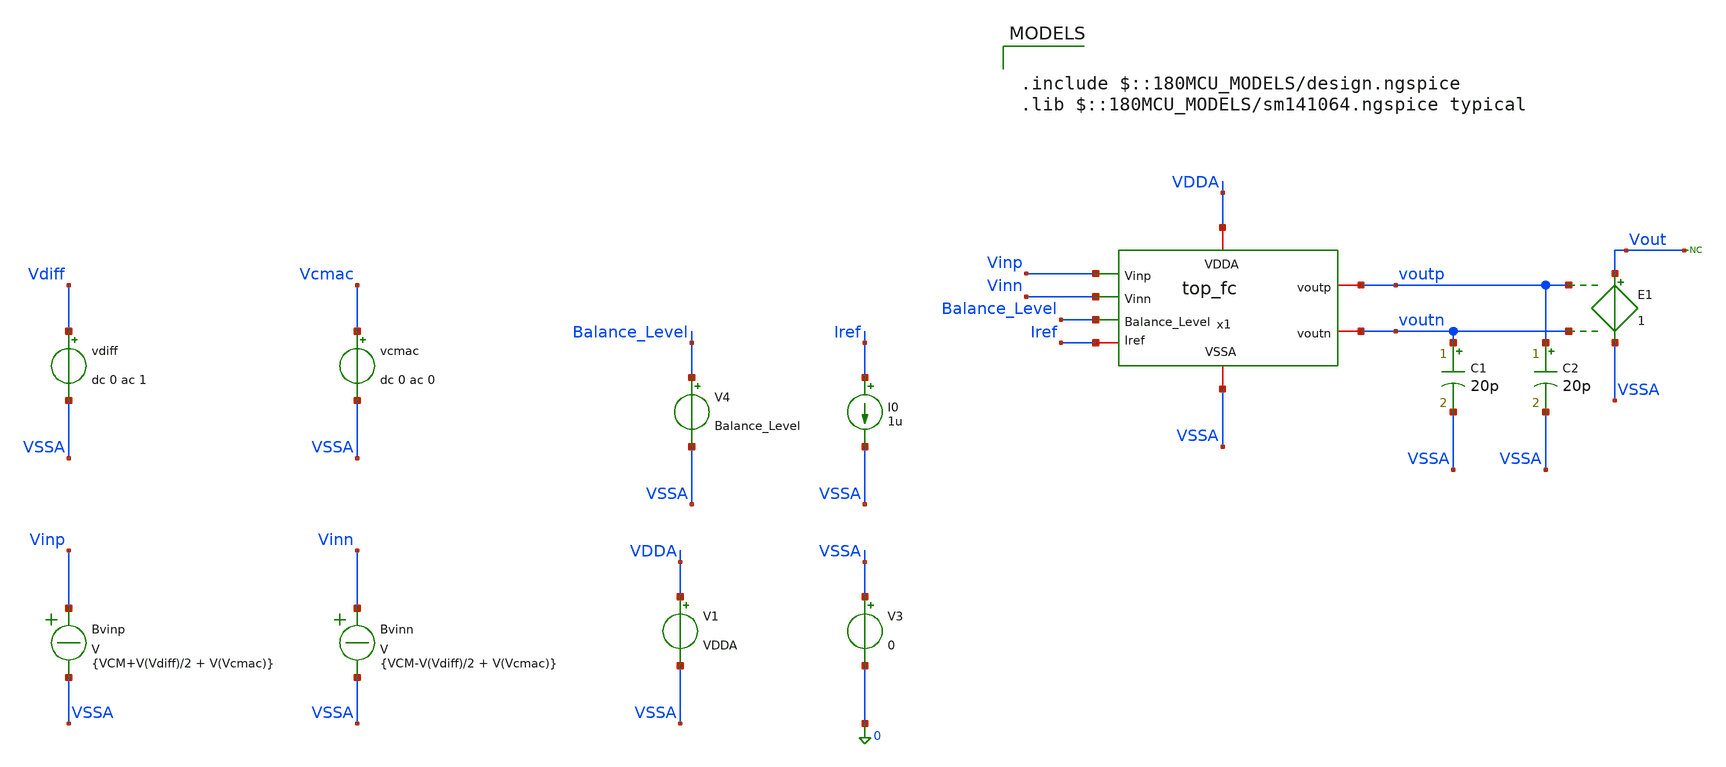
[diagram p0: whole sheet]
** sch_path: Folded_cascode/testbenches/top_fc_cmrr_tb.sch
**.subckt top_fc_cmrr_tb
x1 Balance_Level Vinp voutp VDDA voutn Vinn Iref VSSA top_fc
C1 voutn VSSA 20p m=1
C2 voutp VSSA 20p m=1
V1 VDDA VSSA VDDA
V3 VSSA 0 0
V4 Balance_Level VSSA Balance_Level
I0 Iref VSSA 1u
E1 Vout VSSA voutp voutn 1
* noconn Vout
Bvinp Vinp VSSA V = {VCM+V(Vdiff)/2 + V(Vcmac)}
Bvinn Vinn VSSA V = {VCM-V(Vdiff)/2 + V(Vcmac)}
vdiff Vdiff VSSA dc 0 ac 1
vcmac Vcmac VSSA dc 0 ac 0
**** begin user architecture code

.include $::180MCU_MODELS/design.ngspice
.lib $::180MCU_MODELS/sm141064.ngspice typical



.temp 27
.param VDDA = 5
.param Balance_Level = 1.5
.param VCM = 2.5

.control
option sparse
set filetype=ascii
set wr_singlescale
set wr_vecnames
save all
save @m.x1.x1.xm1.m0[id]
save @m.x1.x1.xm1.m0[gm]
save @m.x1.x1.xm1.m0[vgs]
save @m.x1.x1.xm1.m0[vds]
save @m.x1.x1.xm1.m0[vth]
save @m.x1.x1.xm1.m0[gds]
save @m.x1.x1.xm1.m0[vdsat]

save @m.x1.x1.xm2.m0[id]
save @m.x1.x1.xm2.m0[gm]
save @m.x1.x1.xm2.m0[vgs]
save @m.x1.x1.xm2.m0[vds]
save @m.x1.x1.xm2.m0[vth]
save @m.x1.x1.xm2.m0[gds]
save @m.x1.x1.xm2.m0[vdsat]

save @m.x1.x1.xm9.m0[id]
save @m.x1.x1.xm9.m0[gm]
save @m.x1.x1.xm9.m0[vgs]
save @m.x1.x1.xm9.m0[vds]
save @m.x1.x1.xm9.m0[vth]
save @m.x1.x1.xm9.m0[gds]
save @m.x1.x1.xm9.m0[vdsat]

save @m.x1.x1.xm8.m0[id]
save @m.x1.x1.xm8.m0[gm]
save @m.x1.x1.xm8.m0[vgs]
save @m.x1.x1.xm8.m0[vds]
save @m.x1.x1.xm8.m0[vth]
save @m.x1.x1.xm8.m0[gds]
save @m.x1.x1.xm8.m0[vdsat]

save @m.x1.x1.xm6.m0[id]
save @m.x1.x1.xm6.m0[gm]
save @m.x1.x1.xm6.m0[vgs]
save @m.x1.x1.xm6.m0[vds]
save @m.x1.x1.xm6.m0[vth]
save @m.x1.x1.xm6.m0[gds]
save @m.x1.x1.xm6.m0[vdsat]

save @m.x1.x1.xm5.m0[id]
save @m.x1.x1.xm5.m0[gm]
save @m.x1.x1.xm5.m0[vgs]
save @m.x1.x1.xm5.m0[vds]
save @m.x1.x1.xm5.m0[vth]
save @m.x1.x1.xm5.m0[gds]
save @m.x1.x1.xm5.m0[vdsat]

save @m.x1.x2.xm1.m0[id]
save @m.x1.x2.xm1.m0[gm]
save @m.x1.x2.xm1.m0[vgs]
save @m.x1.x2.xm1.m0[vds]
save @m.x1.x2.xm1.m0[vth]
save @m.x1.x2.xm1.m0[gds]

save @m.x1.x2.xm2.m0[id]
save @m.x1.x2.xm2.m0[gm]
save @m.x1.x2.xm2.m0[vgs]
save @m.x1.x2.xm2.m0[vds]
save @m.x1.x2.xm2.m0[vth]
save @m.x1.x2.xm2.m0[gds]

save @m.x1.x2.xm3.m0[id]
save @m.x1.x2.xm3.m0[gm]
save @m.x1.x2.xm3.m0[vgs]
save @m.x1.x2.xm3.m0[vds]
save @m.x1.x2.xm3.m0[vth]
save @m.x1.x2.xm3.m0[gds]

save @m.x1.x2.xm4.m0[id]
save @m.x1.x2.xm4.m0[gm]
save @m.x1.x2.xm4.m0[vgs]
save @m.x1.x2.xm4.m0[vds]
save @m.x1.x2.xm4.m0[vth]
save @m.x1.x2.xm4.m0[gds]

save @m.x1.x2.xm5.m0[id]
save @m.x1.x2.xm5.m0[gm]
save @m.x1.x2.xm5.m0[vgs]
save @m.x1.x2.xm5.m0[vds]
save @m.x1.x2.xm5.m0[vth]
save @m.x1.x2.xm5.m0[gds]

save @m.x1.x2.xm6.m0[id]
save @m.x1.x2.xm6.m0[gm]
save @m.x1.x2.xm6.m0[vgs]
save @m.x1.x2.xm6.m0[vds]
save @m.x1.x2.xm6.m0[vth]
save @m.x1.x2.xm6.m0[gds]

save @m.x1.x2.xm7.m0[id]
save @m.x1.x2.xm7.m0[gm]
save @m.x1.x2.xm7.m0[vgs]
save @m.x1.x2.xm7.m0[vds]
save @m.x1.x2.xm7.m0[vth]
save @m.x1.x2.xm7.m0[gds]

save @m.x1.x2.xm8.m0[id]
save @m.x1.x2.xm8.m0[gm]
save @m.x1.x2.xm8.m0[vgs]
save @m.x1.x2.xm8.m0[vds]
save @m.x1.x2.xm8.m0[vth]
save @m.x1.x2.xm8.m0[gds]

save @m.x1.x2.xm9.m0[id]
save @m.x1.x2.xm9.m0[gm]
save @m.x1.x2.xm9.m0[vgs]
save @m.x1.x2.xm9.m0[vds]
save @m.x1.x2.xm9.m0[vth]
save @m.x1.x2.xm9.m0[gds]

save @m.x1.x3.xm1.m0[id]
save @m.x1.x3.xm1.m0[gm]
save @m.x1.x3.xm1.m0[vgs]
save @m.x1.x3.xm1.m0[vds]
save @m.x1.x3.xm1.m0[vth]
save @m.x1.x3.xm1.m0[gds]

save @m.x1.x3.xm2.m0[id]
save @m.x1.x3.xm2.m0[gm]
save @m.x1.x3.xm2.m0[vgs]
save @m.x1.x3.xm2.m0[vds]
save @m.x1.x3.xm2.m0[vth]
save @m.x1.x3.xm2.m0[gds]

save @m.x1.x3.xm3.m0[id]
save @m.x1.x3.xm3.m0[gm]
save @m.x1.x3.xm3.m0[vgs]
save @m.x1.x3.xm3.m0[vds]
save @m.x1.x3.xm3.m0[vth]
save @m.x1.x3.xm3.m0[gds]

save @m.x1.x3.xm4.m0[id]
save @m.x1.x3.xm4.m0[gm]
save @m.x1.x3.xm4.m0[vgs]
save @m.x1.x3.xm4.m0[vds]
save @m.x1.x3.xm4.m0[vth]
save @m.x1.x3.xm4.m0[gds]

save @m.x1.x3.xm5.m0[id]
save @m.x1.x3.xm5.m0[gm]
save @m.x1.x3.xm5.m0[vgs]
save @m.x1.x3.xm5.m0[vds]
save @m.x1.x3.xm5.m0[vth]
save @m.x1.x3.xm5.m0[gds]

save @m.x1.x3.xm6.m0[id]
save @m.x1.x3.xm6.m0[gm]
save @m.x1.x3.xm6.m0[vgs]
save @m.x1.x3.xm6.m0[vds]
save @m.x1.x3.xm6.m0[vth]
save @m.x1.x3.xm6.m0[gds]

save @m.x1.x3.xm7.m0[id]
save @m.x1.x3.xm7.m0[gm]
save @m.x1.x3.xm7.m0[vgs]
save @m.x1.x3.xm7.m0[vds]
save @m.x1.x3.xm7.m0[vth]
save @m.x1.x3.xm7.m0[gds]

save @m.x1.x3.xm8.m0[id]
save @m.x1.x3.xm8.m0[gm]
save @m.x1.x3.xm8.m0[vgs]
save @m.x1.x3.xm8.m0[vds]
save @m.x1.x3.xm8.m0[vth]
save @m.x1.x3.xm8.m0[gds]

save @m.x1.x3.xm9.m0[id]
save @m.x1.x3.xm9.m0[gm]
save @m.x1.x3.xm9.m0[vgs]
save @m.x1.x3.xm9.m0[vds]
save @m.x1.x3.xm9.m0[vth]
save @m.x1.x3.xm9.m0[gds]

save @m.x1.x3.xm10.m0[id]
save @m.x1.x3.xm10.m0[gm]
save @m.x1.x3.xm10.m0[vgs]
save @m.x1.x3.xm10.m0[vds]
save @m.x1.x3.xm10.m0[vth]
save @m.x1.x3.xm10.m0[gds]

save @m.x1.x3.xm11.m0[id]
save @m.x1.x3.xm11.m0[gm]
save @m.x1.x3.xm11.m0[vgs]
save @m.x1.x3.xm11.m0[vds]
save @m.x1.x3.xm11.m0[vth]
save @m.x1.x3.xm11.m0[gds]

save @m.x1.x3.xm12.m0[id]
save @m.x1.x3.xm12.m0[gm]
save @m.x1.x3.xm12.m0[vgs]
save @m.x1.x3.xm12.m0[vds]
save @m.x1.x3.xm12.m0[vth]
save @m.x1.x3.xm12.m0[gds]

save @m.x1.x3.xm13.m0[id]
save @m.x1.x3.xm13.m0[gm]
save @m.x1.x3.xm13.m0[vgs]
save @m.x1.x3.xm13.m0[vds]
save @m.x1.x3.xm13.m0[vth]
save @m.x1.x3.xm13.m0[gds]

save @m.x1.x3.xm14.m0[id]
save @m.x1.x3.xm14.m0[gm]
save @m.x1.x3.xm14.m0[vgs]
save @m.x1.x3.xm14.m0[vds]
save @m.x1.x3.xm14.m0[vth]
save @m.x1.x3.xm14.m0[gds]

save @m.x1.x3.xm15.m0[id]
save @m.x1.x3.xm15.m0[gm]
save @m.x1.x3.xm15.m0[vgs]
save @m.x1.x3.xm15.m0[vds]
save @m.x1.x3.xm15.m0[vth]
save @m.x1.x3.xm15.m0[gds]

save @m.x1.x3.xm16.m0[id]
save @m.x1.x3.xm16.m0[gm]
save @m.x1.x3.xm16.m0[vgs]
save @m.x1.x3.xm16.m0[vds]
save @m.x1.x3.xm16.m0[vth]
save @m.x1.x3.xm16.m0[gds]

save @m.x1.x3.xm17.m0[id]
save @m.x1.x3.xm17.m0[gm]
save @m.x1.x3.xm17.m0[vgs]
save @m.x1.x3.xm17.m0[vds]
save @m.x1.x3.xm17.m0[vth]
save @m.x1.x3.xm17.m0[gds]

save @m.x1.x3.xm18.m0[id]
save @m.x1.x3.xm18.m0[gm]
save @m.x1.x3.xm18.m0[vgs]
save @m.x1.x3.xm18.m0[vds]
save @m.x1.x3.xm18.m0[vth]
save @m.x1.x3.xm18.m0[gds]

save @m.x1.x3.xm21.m0[id]
save @m.x1.x3.xm21.m0[gm]
save @m.x1.x3.xm21.m0[vgs]
save @m.x1.x3.xm21.m0[vds]
save @m.x1.x3.xm21.m0[vth]
save @m.x1.x3.xm21.m0[gds]

save @m.x1.x3.xm22.m0[id]
save @m.x1.x3.xm22.m0[gm]
save @m.x1.x3.xm22.m0[vgs]
save @m.x1.x3.xm22.m0[vds]
save @m.x1.x3.xm22.m0[vth]
save @m.x1.x3.xm22.m0[gds]

op
write top_fc_op_tb.raw all

* ============================================================
* 1. DIFFERENTIAL-MODE GAIN
*
* Vdiff = AC 1
* Vcmac = AC 0
*
* Vinp = VCM + Vdiff/2
* Vinn = VCM - Vdiff/2
*
* Therefore:
*
* Vinp - Vinn = Vdiff = 1 V AC
* ============================================================

alter @Vdiff[acmag] = 1
alter @Vcmac[acmag] = 0

ac dec 100 1 1G

* Differential output
let vod = v(voutp)-v(voutn)

* Differential voltage gain
let ad = vod/v(Vdiff)
let ad_db = db(ad)

* ------------------------------------------------------------
* Differential gain measurements
* ------------------------------------------------------------

meas ac ad_1Hz   FIND ad_db AT=1
meas ac ad_1k    FIND ad_db AT=1k
meas ac ad_10k   FIND ad_db AT=10k
meas ac ad_100k  FIND ad_db AT=100k
meas ac ad_1Meg  FIND ad_db AT=1Meg
meas ac ad_10Meg FIND ad_db AT=10Meg

print ad_1Hz
print ad_1k
print ad_10k
print ad_100k
print ad_1Meg
print ad_10Meg

write fc_cmfb_cmrr_diff_tb.raw

* ============================================================
* 2. COMMON-MODE GAIN
*
* Vdiff = AC 0
* Vcmac = AC 1
*
* Vinp = VCM + Vcmac
* Vinn = VCM + Vcmac
*
* Therefore:
*
* Vinp = Vinn
* Vicm = 1 V AC
* ============================================================

alter @Vdiff[acmag] = 0
alter @Vcmac[acmag] = 1

ac dec 100 1 1G

* Differential output caused by common-mode excitation
let vod_cm = v(voutp)-v(voutn)

* Common-mode to differential gain
let acm = vod_cm/v(Vcmac)
let acm_db = db(acm)

* ------------------------------------------------------------
* Common-mode gain measurements
* ------------------------------------------------------------

meas ac acm_1Hz   FIND acm_db AT=1
meas ac acm_1k    FIND acm_db AT=1k
meas ac acm_10k   FIND acm_db AT=10k
meas ac acm_100k  FIND acm_db AT=100k
meas ac acm_1Meg  FIND acm_db AT=1Meg
meas ac acm_10Meg FIND acm_db AT=10Meg

print acm_1Hz
print acm_1k
print acm_10k
print acm_100k
print acm_1Meg
print acm_10Meg

* ============================================================
* 3. CMRR
*
* First AC analysis  -> plot ac1
* Second AC analysis -> plot ac2 (current plot)
*
* CMRR[dB] = Ad[dB] - Acm[dB]
* ============================================================

let cmrr_db = ac1.ad_db - acm_db

* ------------------------------------------------------------
* CMRR measurements
* ------------------------------------------------------------

meas ac cmrr_1Hz   FIND cmrr_db AT=1
meas ac cmrr_1k    FIND cmrr_db AT=1k
meas ac cmrr_10k   FIND cmrr_db AT=10k
meas ac cmrr_100k  FIND cmrr_db AT=100k
meas ac cmrr_1Meg  FIND cmrr_db AT=1Meg
meas ac cmrr_10Meg FIND cmrr_db AT=10Meg

print cmrr_1Hz
print cmrr_1k
print cmrr_10k
print cmrr_100k
print cmrr_1Meg
print cmrr_10Meg

* ============================================================
* Save common-mode / CMRR results
* ============================================================

write top_fc_cmrr_tb.raw

* ============================================================
* Plots
* ============================================================

* Common-mode gain
plot acm_db

* CMRR
plot cmrr_db

* Differential gain from first AC run
plot ac1.ad_db

.endc


**** end user architecture code
**.ends
.end
